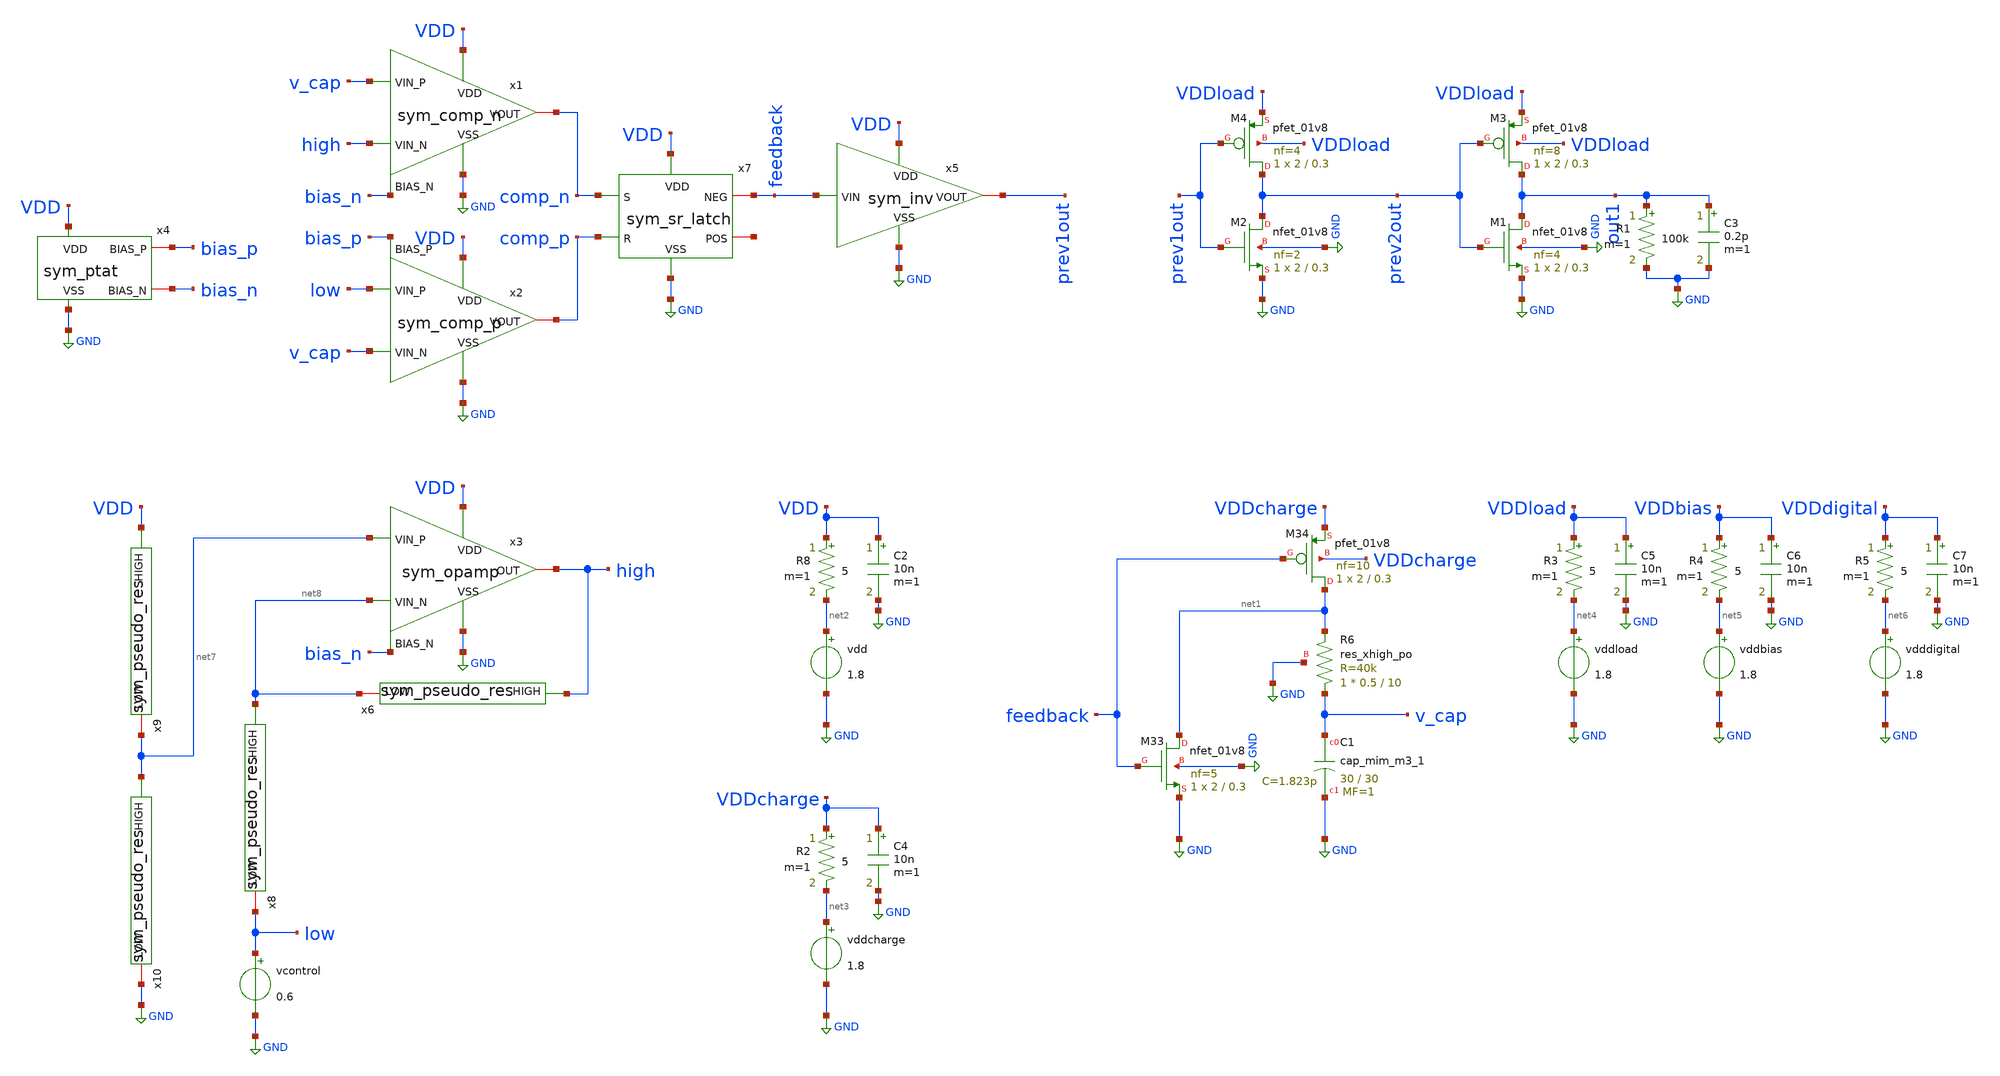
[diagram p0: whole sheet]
** sch_path: schem/tb/tb_full.sch
**.subckt tb_full
XC1 v_cap GND sky130_fd_pr__cap_mim_m3_1 W=30 L=30 MF=1 m=1
XM33 net1 feedback GND GND sky130_fd_pr__nfet_01v8 L=0.3 W=2 nf=5 ad='int((5 + 1)/2) * 2 / 5 * 0.29'
+ as='int((5 + 2)/2) * 2 / 5 * 0.29' pd='2*int((5 + 1)/2) * (2 / 5 + 0.29)' ps='2*int((5 + 2)/2) * (2 / 5 + 0.29)'
+ nrd='0.29 / 2 ' nrs='0.29 / 2 ' sa=0 sb=0 sd=0 mult=1 m=1
XM34 net1 feedback VDDcharge VDDcharge sky130_fd_pr__pfet_01v8 L=0.3 W=2 nf=10 ad='int((10 + 1)/2) * 2 / 10 * 0.29'
+ as='int((10 + 2)/2) * 2 / 10 * 0.29' pd='2*int((10 + 1)/2) * (2 / 10 + 0.29)' ps='2*int((10 + 2)/2) * (2 / 10 + 0.29)'
+ nrd='0.29 / 2 ' nrs='0.29 / 2 ' sa=0 sb=0 sd=0 mult=1 m=1
vdd net2 GND 1.8
C2 VDD GND 10n m=1
R8 VDD net2 5 m=1
vddcharge net3 GND 1.8
C4 VDDcharge GND 10n m=1
R2 VDDcharge net3 5 m=1
R1 out1 GND 100k m=1
C3 out1 GND 0.2p m=1
vddload net4 GND 1.8
C5 VDDload GND 10n m=1
R3 VDDload net4 5 m=1
vddbias net5 GND 1.8
C6 VDDbias GND 10n m=1
R4 VDDbias net5 5 m=1
vdddigital net6 GND 1.8
C7 VDDdigital GND 10n m=1
R5 VDDdigital net6 5 m=1
XM1 out1 prev2out GND GND sky130_fd_pr__nfet_01v8 L=0.3 W=2 nf=4 ad='int((4 + 1)/2) * 2 / 4 * 0.29' as='int((4 + 2)/2) * 2 / 4 * 0.29'
+ pd='2*int((4 + 1)/2) * (2 / 4 + 0.29)' ps='2*int((4 + 2)/2) * (2 / 4 + 0.29)' nrd='0.29 / 2 ' nrs='0.29 / 2 '
+ sa=0 sb=0 sd=0 mult=1 m=1
XM3 out1 prev2out VDDload VDDload sky130_fd_pr__pfet_01v8 L=0.3 W=2 nf=8 ad='int((8 + 1)/2) * 2 / 8 * 0.29'
+ as='int((8 + 2)/2) * 2 / 8 * 0.29' pd='2*int((8 + 1)/2) * (2 / 8 + 0.29)' ps='2*int((8 + 2)/2) * (2 / 8 + 0.29)'
+ nrd='0.29 / 2 ' nrs='0.29 / 2 ' sa=0 sb=0 sd=0 mult=1 m=1
XM2 prev2out prev1out GND GND sky130_fd_pr__nfet_01v8 L=0.3 W=2 nf=2 ad='int((2 + 1)/2) * 2 / 2 * 0.29'
+ as='int((2 + 2)/2) * 2 / 2 * 0.29' pd='2*int((2 + 1)/2) * (2 / 2 + 0.29)' ps='2*int((2 + 2)/2) * (2 / 2 + 0.29)'
+ nrd='0.29 / 2 ' nrs='0.29 / 2 ' sa=0 sb=0 sd=0 mult=1 m=1
XM4 prev2out prev1out VDDload VDDload sky130_fd_pr__pfet_01v8 L=0.3 W=2 nf=4 ad='int((4 + 1)/2) * 2 / 4 * 0.29'
+ as='int((4 + 2)/2) * 2 / 4 * 0.29' pd='2*int((4 + 1)/2) * (2 / 4 + 0.29)' ps='2*int((4 + 2)/2) * (2 / 4 + 0.29)'
+ nrd='0.29 / 2 ' nrs='0.29 / 2 ' sa=0 sb=0 sd=0 mult=1 m=1
XR6 v_cap net1 GND sky130_fd_pr__res_xhigh_po W=0.5 L=10 mult=1 m=1
vcontrol low GND 0.6
x4 VDD GND bias_p bias_n sym_ptat
x9 VDD net7 sym_pseudo_res
x10 net7 GND sym_pseudo_res
x8 net8 low sym_pseudo_res
x6 high net8 sym_pseudo_res
x3 VDD GND net7 net8 high bias_n sym_opamp
x1 VDD GND high v_cap comp_n bias_n sym_comp_n
x2 VDD GND bias_p comp_p low v_cap sym_comp_p
x5 VDD feedback prev1out GND sym_inv
x7 VDD GND comp_p comp_n feedback net9 sym_sr_latch
**** begin user architecture code


.lib /usr/local/share/pdk/sky130A/libs.tech/ngspice/sky130.lib.spice tt

.tran 0.1n 2u
.save all

.control
    run

    * Find rising edges of feedback signal (threshold at 0.9V for 1.8V signal)
    meas tran t1 when feedback=0.9 rise=2
    meas tran t2 when feedback=0.9 rise=3

    * Calculate period and frequency from 2nd period onwards
    let period = t2 - t1
    let freq = 1 / period

    print period
    print freq

    plot low high v_cap prev1out out1
    plot abs(i(vdd))*1.8 + abs(i(vddcharge))*1.8
.endc

.end


**** end user architecture code
**.ends

* expanding   symbol:  /home/zhixuan/projects/fyp_vco/schem/symbol_repo/sym_ptat.sym # of pins=4
** sym_path: schem/symbol_repo/sym_ptat.sym
** sch_path: schem/symbol_repo/sym_ptat.sch
.subckt sym_ptat VDD VSS BIAS_P BIAS_N
*.ipin VDD
*.ipin VSS
*.iopin BIAS_P
*.iopin BIAS_N
XMN_ptat2 net6 net1 net2 VSS sky130_fd_pr__nfet_01v8 L=0.5 W=2 nf=2 ad='int((2 + 1)/2) * 2 / 2 * 0.29'
+ as='int((2 + 2)/2) * 2 / 2 * 0.29' pd='2*int((2 + 1)/2) * (2 / 2 + 0.29)' ps='2*int((2 + 2)/2) * (2 / 2 + 0.29)'
+ nrd='0.29 / 2 ' nrs='0.29 / 2 ' sa=0 sb=0 sd=0 mult=1 m=1
XMP_diode1 net3 BIAS_P VDD VDD sky130_fd_pr__pfet_01v8 L=0.5 W=2 nf=2 ad='int((2 + 1)/2) * 2 / 2 * 0.29'
+ as='int((2 + 2)/2) * 2 / 2 * 0.29' pd='2*int((2 + 1)/2) * (2 / 2 + 0.29)' ps='2*int((2 + 2)/2) * (2 / 2 + 0.29)'
+ nrd='0.29 / 2 ' nrs='0.29 / 2 ' sa=0 sb=0 sd=0 mult=1 m=1
XMP_mir1_l net4 BIAS_P VDD VDD sky130_fd_pr__pfet_01v8 L=0.5 W=2 nf=2 ad='int((2 + 1)/2) * 2 / 2 * 0.29'
+ as='int((2 + 2)/2) * 2 / 2 * 0.29' pd='2*int((2 + 1)/2) * (2 / 2 + 0.29)' ps='2*int((2 + 2)/2) * (2 / 2 + 0.29)'
+ nrd='0.29 / 2 ' nrs='0.29 / 2 ' sa=0 sb=0 sd=0 mult=1 m=1
XMN_diode2 net5 net1 VSS VSS sky130_fd_pr__nfet_01v8 L=0.5 W=2 nf=4 ad='int((4 + 1)/2) * 2 / 4 * 0.29'
+ as='int((4 + 2)/2) * 2 / 4 * 0.29' pd='2*int((4 + 1)/2) * (2 / 4 + 0.29)' ps='2*int((4 + 2)/2) * (2 / 4 + 0.29)'
+ nrd='0.29 / 2 ' nrs='0.29 / 2 ' sa=0 sb=0 sd=0 mult=1 m=1
XMP_inv BIAS_N BIAS_P VDD VDD sky130_fd_pr__pfet_01v8 L=0.75 W=2 nf=5 ad='int((5 + 1)/2) * 2 / 5 * 0.29'
+ as='int((5 + 2)/2) * 2 / 5 * 0.29' pd='2*int((5 + 1)/2) * (2 / 5 + 0.29)' ps='2*int((5 + 2)/2) * (2 / 5 + 0.29)'
+ nrd='0.29 / 2 ' nrs='0.29 / 2 ' sa=0 sb=0 sd=0 mult=1 m=1
XMP_diode2 BIAS_P BIAS_P net3 VDD sky130_fd_pr__pfet_01v8 L=0.5 W=2 nf=2 ad='int((2 + 1)/2) * 2 / 2 * 0.29'
+ as='int((2 + 2)/2) * 2 / 2 * 0.29' pd='2*int((2 + 1)/2) * (2 / 2 + 0.29)' ps='2*int((2 + 2)/2) * (2 / 2 + 0.29)'
+ nrd='0.29 / 2 ' nrs='0.29 / 2 ' sa=0 sb=0 sd=0 mult=1 m=1
XMP_mir2_l net1 BIAS_P net4 VDD sky130_fd_pr__pfet_01v8 L=0.5 W=2 nf=2 ad='int((2 + 1)/2) * 2 / 2 * 0.29'
+ as='int((2 + 2)/2) * 2 / 2 * 0.29' pd='2*int((2 + 1)/2) * (2 / 2 + 0.29)' ps='2*int((2 + 2)/2) * (2 / 2 + 0.29)'
+ nrd='0.29 / 2 ' nrs='0.29 / 2 ' sa=0 sb=0 sd=0 mult=1 m=1
XMN_ptat1 BIAS_P net1 net6 VSS sky130_fd_pr__nfet_01v8 L=0.5 W=2 nf=2 ad='int((2 + 1)/2) * 2 / 2 * 0.29'
+ as='int((2 + 2)/2) * 2 / 2 * 0.29' pd='2*int((2 + 1)/2) * (2 / 2 + 0.29)' ps='2*int((2 + 2)/2) * (2 / 2 + 0.29)'
+ nrd='0.29 / 2 ' nrs='0.29 / 2 ' sa=0 sb=0 sd=0 mult=1 m=1
XMN_diode1 net1 net1 net5 VSS sky130_fd_pr__nfet_01v8 L=0.5 W=2 nf=4 ad='int((4 + 1)/2) * 2 / 4 * 0.29'
+ as='int((4 + 2)/2) * 2 / 4 * 0.29' pd='2*int((4 + 1)/2) * (2 / 4 + 0.29)' ps='2*int((4 + 2)/2) * (2 / 4 + 0.29)'
+ nrd='0.29 / 2 ' nrs='0.29 / 2 ' sa=0 sb=0 sd=0 mult=1 m=1
XMN_inv BIAS_N BIAS_N VSS VSS sky130_fd_pr__nfet_01v8 L=0.75 W=2.5 nf=2 ad='int((2 + 1)/2) * 2.5 / 2 * 0.29'
+ as='int((2 + 2)/2) * 2.5 / 2 * 0.29' pd='2*int((2 + 1)/2) * (2.5 / 2 + 0.29)' ps='2*int((2 + 2)/2) * (2.5 / 2 + 0.29)'
+ nrd='0.29 / 2.5 ' nrs='0.29 / 2.5 ' sa=0 sb=0 sd=0 mult=1 m=1
XR1 VSS net2 VSS sky130_fd_pr__res_xhigh_po_0p35 L=2.8 mult=1 m=1
XMP_startup net1 VSS VDD VDD sky130_fd_pr__pfet_01v8 L=13 W=1 nf=1 ad='int((1 + 1)/2) * 1 / 1 * 0.29'
+ as='int((1 + 2)/2) * 1 / 1 * 0.29' pd='2*int((1 + 1)/2) * (1 / 1 + 0.29)' ps='2*int((1 + 2)/2) * (1 / 1 + 0.29)'
+ nrd='0.29 / 1 ' nrs='0.29 / 1 ' sa=0 sb=0 sd=0 mult=1 m=1
XMN_diode3 net7 net1 VSS VSS sky130_fd_pr__nfet_01v8 L=0.5 W=2 nf=4 ad='int((4 + 1)/2) * 2 / 4 * 0.29'
+ as='int((4 + 2)/2) * 2 / 4 * 0.29' pd='2*int((4 + 1)/2) * (2 / 4 + 0.29)' ps='2*int((4 + 2)/2) * (2 / 4 + 0.29)'
+ nrd='0.29 / 2 ' nrs='0.29 / 2 ' sa=0 sb=0 sd=0 mult=1 m=1
XMN_diode4 net1 net1 net7 VSS sky130_fd_pr__nfet_01v8 L=0.5 W=2 nf=4 ad='int((4 + 1)/2) * 2 / 4 * 0.29'
+ as='int((4 + 2)/2) * 2 / 4 * 0.29' pd='2*int((4 + 1)/2) * (2 / 4 + 0.29)' ps='2*int((4 + 2)/2) * (2 / 4 + 0.29)'
+ nrd='0.29 / 2 ' nrs='0.29 / 2 ' sa=0 sb=0 sd=0 mult=1 m=1
.ends


* expanding   symbol:  /home/zhixuan/projects/fyp_vco/schem/symbol_repo/sym_pseudo_res.sym # of
*+ pins=2
** sym_path: schem/symbol_repo/sym_pseudo_res.sym
** sch_path: schem/symbol_repo/sym_pseudo_res.sch
.subckt sym_pseudo_res HIGH LOW
*.iopin LOW
*.ipin HIGH
XMP_r1 net1 net1 HIGH HIGH sky130_fd_pr__pfet_01v8 L=0.15 W=1 nf=1 ad='int((1 + 1)/2) * 1 / 1 * 0.29'
+ as='int((1 + 2)/2) * 1 / 1 * 0.29' pd='2*int((1 + 1)/2) * (1 / 1 + 0.29)' ps='2*int((1 + 2)/2) * (1 / 1 + 0.29)'
+ nrd='0.29 / 1 ' nrs='0.29 / 1 ' sa=0 sb=0 sd=0 mult=1 m=1
XMP_r2 LOW LOW net1 HIGH sky130_fd_pr__pfet_01v8 L=0.15 W=1 nf=1 ad='int((1 + 1)/2) * 1 / 1 * 0.29' as='int((1 + 2)/2) * 1 / 1 * 0.29'
+ pd='2*int((1 + 1)/2) * (1 / 1 + 0.29)' ps='2*int((1 + 2)/2) * (1 / 1 + 0.29)' nrd='0.29 / 1 ' nrs='0.29 / 1 '
+ sa=0 sb=0 sd=0 mult=1 m=1
.ends


* expanding   symbol:  /home/zhixuan/projects/fyp_vco/schem/symbol_repo/sym_opamp.sym # of pins=6
** sym_path: schem/symbol_repo/sym_opamp.sym
** sch_path: schem/symbol_repo/sym_opamp.sch
.subckt sym_opamp VDD VSS VIN_P VIN_N OUT BIAS_N
*.ipin VDD
*.ipin VSS
*.ipin BIAS_N
*.iopin OUT
*.ipin VIN_N
*.ipin VIN_P
XMN_vinn net1 VIN_N net3 VSS sky130_fd_pr__nfet_01v8 L=0.5 W=1 nf=1 ad='int((1 + 1)/2) * 1 / 1 * 0.29'
+ as='int((1 + 2)/2) * 1 / 1 * 0.29' pd='2*int((1 + 1)/2) * (1 / 1 + 0.29)' ps='2*int((1 + 2)/2) * (1 / 1 + 0.29)'
+ nrd='0.29 / 1 ' nrs='0.29 / 1 ' sa=0 sb=0 sd=0 mult=1 m=1
XMP_cs_1 net2 net1 VDD VDD sky130_fd_pr__pfet_01v8 L=0.5 W=2 nf=1 ad='int((1 + 1)/2) * 2 / 1 * 0.29'
+ as='int((1 + 2)/2) * 2 / 1 * 0.29' pd='2*int((1 + 1)/2) * (2 / 1 + 0.29)' ps='2*int((1 + 2)/2) * (2 / 1 + 0.29)'
+ nrd='0.29 / 2 ' nrs='0.29 / 2 ' sa=0 sb=0 sd=0 mult=1 m=1
XMP_diode net1 net1 VDD VDD sky130_fd_pr__pfet_01v8 L=0.5 W=2 nf=1 ad='int((1 + 1)/2) * 2 / 1 * 0.29'
+ as='int((1 + 2)/2) * 2 / 1 * 0.29' pd='2*int((1 + 1)/2) * (2 / 1 + 0.29)' ps='2*int((1 + 2)/2) * (2 / 1 + 0.29)'
+ nrd='0.29 / 2 ' nrs='0.29 / 2 ' sa=0 sb=0 sd=0 mult=1 m=1
XMN_vinp net2 VIN_P net3 VSS sky130_fd_pr__nfet_01v8 L=0.5 W=1 nf=1 ad='int((1 + 1)/2) * 1 / 1 * 0.29'
+ as='int((1 + 2)/2) * 1 / 1 * 0.29' pd='2*int((1 + 1)/2) * (1 / 1 + 0.29)' ps='2*int((1 + 2)/2) * (1 / 1 + 0.29)'
+ nrd='0.29 / 1 ' nrs='0.29 / 1 ' sa=0 sb=0 sd=0 mult=1 m=1
XMN_tail_1 net3 BIAS_N VSS GND sky130_fd_pr__nfet_01v8 L=0.75 W=2 nf=1 ad='int((1 + 1)/2) * 2 / 1 * 0.29'
+ as='int((1 + 2)/2) * 2 / 1 * 0.29' pd='2*int((1 + 1)/2) * (2 / 1 + 0.29)' ps='2*int((1 + 2)/2) * (2 / 1 + 0.29)'
+ nrd='0.29 / 2 ' nrs='0.29 / 2 ' sa=0 sb=0 sd=0 mult=1 m=1
XMP_cs_2 OUT net2 VDD VDD sky130_fd_pr__pfet_01v8 L=0.5 W=2 nf=1 ad='int((1 + 1)/2) * 2 / 1 * 0.29' as='int((1 + 2)/2) * 2 / 1 * 0.29'
+ pd='2*int((1 + 1)/2) * (2 / 1 + 0.29)' ps='2*int((1 + 2)/2) * (2 / 1 + 0.29)' nrd='0.29 / 2 ' nrs='0.29 / 2 '
+ sa=0 sb=0 sd=0 mult=1 m=1
XMN_tail_2 OUT BIAS_N VSS VSS sky130_fd_pr__nfet_01v8 L=0.75 W=2 nf=1 ad='int((1 + 1)/2) * 2 / 1 * 0.29'
+ as='int((1 + 2)/2) * 2 / 1 * 0.29' pd='2*int((1 + 1)/2) * (2 / 1 + 0.29)' ps='2*int((1 + 2)/2) * (2 / 1 + 0.29)'
+ nrd='0.29 / 2 ' nrs='0.29 / 2 ' sa=0 sb=0 sd=0 mult=1 m=1
XCc net4 OUT sky130_fd_pr__cap_mim_m3_1 W=4 L=4 MF=1 m=1
XR1 net4 net2 VSS sky130_fd_pr__res_xhigh_po_0p35 L=2 mult=1 m=1
.ends


* expanding   symbol:  /home/zhixuan/projects/fyp_vco/schem/symbol_repo/sym_comp_n.sym # of pins=6
** sym_path: schem/symbol_repo/sym_comp_n.sym
** sch_path: schem/symbol_repo/sym_comp_n.sch
.subckt sym_comp_n VDD VSS VIN_N VIN_P VOUT BIAS_N
*.ipin VDD
*.ipin VSS
*.ipin VIN_N
*.ipin VIN_P
*.ipin BIAS_N
*.iopin VOUT
XMP_diode_l net1 net1 VDD VDD sky130_fd_pr__pfet_01v8 L=0.3 W=2 nf=2 ad='int((2 + 1)/2) * 2 / 2 * 0.29'
+ as='int((2 + 2)/2) * 2 / 2 * 0.29' pd='2*int((2 + 1)/2) * (2 / 2 + 0.29)' ps='2*int((2 + 2)/2) * (2 / 2 + 0.29)'
+ nrd='0.29 / 2 ' nrs='0.29 / 2 ' sa=0 sb=0 sd=0 mult=1 m=1
XMP_cs_l net2 net1 VDD VDD sky130_fd_pr__pfet_01v8 L=0.3 W=2 nf=2 ad='int((2 + 1)/2) * 2 / 2 * 0.29'
+ as='int((2 + 2)/2) * 2 / 2 * 0.29' pd='2*int((2 + 1)/2) * (2 / 2 + 0.29)' ps='2*int((2 + 2)/2) * (2 / 2 + 0.29)'
+ nrd='0.29 / 2 ' nrs='0.29 / 2 ' sa=0 sb=0 sd=0 mult=1 m=1
XMP_cs_r net1 net2 VDD VDD sky130_fd_pr__pfet_01v8 L=0.3 W=2 nf=2 ad='int((2 + 1)/2) * 2 / 2 * 0.29'
+ as='int((2 + 2)/2) * 2 / 2 * 0.29' pd='2*int((2 + 1)/2) * (2 / 2 + 0.29)' ps='2*int((2 + 2)/2) * (2 / 2 + 0.29)'
+ nrd='0.29 / 2 ' nrs='0.29 / 2 ' sa=0 sb=0 sd=0 mult=1 m=1
XMP_diode_r net2 net2 VDD VDD sky130_fd_pr__pfet_01v8 L=0.3 W=2 nf=2 ad='int((2 + 1)/2) * 2 / 2 * 0.29'
+ as='int((2 + 2)/2) * 2 / 2 * 0.29' pd='2*int((2 + 1)/2) * (2 / 2 + 0.29)' ps='2*int((2 + 2)/2) * (2 / 2 + 0.29)'
+ nrd='0.29 / 2 ' nrs='0.29 / 2 ' sa=0 sb=0 sd=0 mult=1 m=1
XMN_vinn net1 VIN_N net3 VSS sky130_fd_pr__nfet_01v8 L=0.5 W=2.5 nf=1 ad='int((1 + 1)/2) * 2.5 / 1 * 0.29'
+ as='int((1 + 2)/2) * 2.5 / 1 * 0.29' pd='2*int((1 + 1)/2) * (2.5 / 1 + 0.29)' ps='2*int((1 + 2)/2) * (2.5 / 1 + 0.29)'
+ nrd='0.29 / 2.5 ' nrs='0.29 / 2.5 ' sa=0 sb=0 sd=0 mult=1 m=1
XMN_vinp net2 VIN_P net3 VSS sky130_fd_pr__nfet_01v8 L=0.5 W=2.5 nf=1 ad='int((1 + 1)/2) * 2.5 / 1 * 0.29'
+ as='int((1 + 2)/2) * 2.5 / 1 * 0.29' pd='2*int((1 + 1)/2) * (2.5 / 1 + 0.29)' ps='2*int((1 + 2)/2) * (2.5 / 1 + 0.29)'
+ nrd='0.29 / 2.5 ' nrs='0.29 / 2.5 ' sa=0 sb=0 sd=0 mult=1 m=1
XMN_tail net3 BIAS_N VSS VSS sky130_fd_pr__nfet_01v8 L=0.75 W=2.5 nf=2 ad='int((2 + 1)/2) * 2.5 / 2 * 0.29'
+ as='int((2 + 2)/2) * 2.5 / 2 * 0.29' pd='2*int((2 + 1)/2) * (2.5 / 2 + 0.29)' ps='2*int((2 + 2)/2) * (2.5 / 2 + 0.29)'
+ nrd='0.29 / 2.5 ' nrs='0.29 / 2.5 ' sa=0 sb=0 sd=0 mult=1 m=1
XMP_latch_r VOUT net2 VDD VDD sky130_fd_pr__pfet_01v8 L=0.15 W=0.5 nf=1 ad='int((1 + 1)/2) * 0.5 / 1 * 0.29'
+ as='int((1 + 2)/2) * 0.5 / 1 * 0.29' pd='2*int((1 + 1)/2) * (0.5 / 1 + 0.29)' ps='2*int((1 + 2)/2) * (0.5 / 1 + 0.29)'
+ nrd='0.29 / 0.5 ' nrs='0.29 / 0.5 ' sa=0 sb=0 sd=0 mult=1 m=1
XMP_latch_l net5 net1 VDD VDD sky130_fd_pr__pfet_01v8 L=0.15 W=0.5 nf=1 ad='int((1 + 1)/2) * 0.5 / 1 * 0.29'
+ as='int((1 + 2)/2) * 0.5 / 1 * 0.29' pd='2*int((1 + 1)/2) * (0.5 / 1 + 0.29)' ps='2*int((1 + 2)/2) * (0.5 / 1 + 0.29)'
+ nrd='0.29 / 0.5 ' nrs='0.29 / 0.5 ' sa=0 sb=0 sd=0 mult=1 m=1
XMN_latch_r VOUT net4 VSS VSS sky130_fd_pr__nfet_01v8 L=0.15 W=0.5 nf=1 ad='int((1 + 1)/2) * 0.5 / 1 * 0.29'
+ as='int((1 + 2)/2) * 0.5 / 1 * 0.29' pd='2*int((1 + 1)/2) * (0.5 / 1 + 0.29)' ps='2*int((1 + 2)/2) * (0.5 / 1 + 0.29)'
+ nrd='0.29 / 0.5 ' nrs='0.29 / 0.5 ' sa=0 sb=0 sd=0 mult=1 m=1
XMN_diode_l net4 net4 VSS VSS sky130_fd_pr__nfet_01v8 L=0.15 W=0.5 nf=1 ad='int((1 + 1)/2) * 0.5 / 1 * 0.29'
+ as='int((1 + 2)/2) * 0.5 / 1 * 0.29' pd='2*int((1 + 1)/2) * (0.5 / 1 + 0.29)' ps='2*int((1 + 2)/2) * (0.5 / 1 + 0.29)'
+ nrd='0.29 / 0.5 ' nrs='0.29 / 0.5 ' sa=0 sb=0 sd=0 mult=1 m=1
XMP_lim net4 net4 net5 VDD sky130_fd_pr__pfet_01v8 L=0.15 W=0.5 nf=1 ad='int((1 + 1)/2) * 0.5 / 1 * 0.29'
+ as='int((1 + 2)/2) * 0.5 / 1 * 0.29' pd='2*int((1 + 1)/2) * (0.5 / 1 + 0.29)' ps='2*int((1 + 2)/2) * (0.5 / 1 + 0.29)'
+ nrd='0.29 / 0.5 ' nrs='0.29 / 0.5 ' sa=0 sb=0 sd=0 mult=1 m=1
.ends


* expanding   symbol:  /home/zhixuan/projects/fyp_vco/schem/symbol_repo/sym_comp_p.sym # of pins=6
** sym_path: schem/symbol_repo/sym_comp_p.sym
** sch_path: schem/symbol_repo/sym_comp_p.sch
.subckt sym_comp_p VDD VSS BIAS_P VOUT VIN_P VIN_N
*.ipin VDD
*.ipin VSS
*.ipin BIAS_P
*.ipin VIN_N
*.ipin VIN_P
*.iopin VOUT
XMN_cs_l net2 net1 VSS VSS sky130_fd_pr__nfet_01v8 L=0.15 W=1 nf=1 ad='int((1 + 1)/2) * 1 / 1 * 0.29'
+ as='int((1 + 2)/2) * 1 / 1 * 0.29' pd='2*int((1 + 1)/2) * (1 / 1 + 0.29)' ps='2*int((1 + 2)/2) * (1 / 1 + 0.29)'
+ nrd='0.29 / 1 ' nrs='0.29 / 1 ' sa=0 sb=0 sd=0 mult=1 m=1
XMP_tail net4 BIAS_P VDD VDD sky130_fd_pr__pfet_01v8 L=0.75 W=2 nf=5 ad='int((5 + 1)/2) * 2 / 5 * 0.29'
+ as='int((5 + 2)/2) * 2 / 5 * 0.29' pd='2*int((5 + 1)/2) * (2 / 5 + 0.29)' ps='2*int((5 + 2)/2) * (2 / 5 + 0.29)'
+ nrd='0.29 / 2 ' nrs='0.29 / 2 ' sa=0 sb=0 sd=0 mult=1 m=1
XMP_vinn net1 VIN_N net4 VDD sky130_fd_pr__pfet_01v8 L=0.5 W=2.5 nf=2 ad='int((2 + 1)/2) * 2.5 / 2 * 0.29'
+ as='int((2 + 2)/2) * 2.5 / 2 * 0.29' pd='2*int((2 + 1)/2) * (2.5 / 2 + 0.29)' ps='2*int((2 + 2)/2) * (2.5 / 2 + 0.29)'
+ nrd='0.29 / 2.5 ' nrs='0.29 / 2.5 ' sa=0 sb=0 sd=0 mult=1 m=1
XMP_vinp net2 VIN_P net4 VDD sky130_fd_pr__pfet_01v8 L=0.5 W=2.5 nf=2 ad='int((2 + 1)/2) * 2.5 / 2 * 0.29'
+ as='int((2 + 2)/2) * 2.5 / 2 * 0.29' pd='2*int((2 + 1)/2) * (2.5 / 2 + 0.29)' ps='2*int((2 + 2)/2) * (2.5 / 2 + 0.29)'
+ nrd='0.29 / 2.5 ' nrs='0.29 / 2.5 ' sa=0 sb=0 sd=0 mult=1 m=1
XMN_diode_l net1 net1 VSS VSS sky130_fd_pr__nfet_01v8 L=0.15 W=1 nf=1 ad='int((1 + 1)/2) * 1 / 1 * 0.29'
+ as='int((1 + 2)/2) * 1 / 1 * 0.29' pd='2*int((1 + 1)/2) * (1 / 1 + 0.29)' ps='2*int((1 + 2)/2) * (1 / 1 + 0.29)'
+ nrd='0.29 / 1 ' nrs='0.29 / 1 ' sa=0 sb=0 sd=0 mult=1 m=1
XMN_diode_r net2 net2 VSS VSS sky130_fd_pr__nfet_01v8 L=0.15 W=1 nf=1 ad='int((1 + 1)/2) * 1 / 1 * 0.29'
+ as='int((1 + 2)/2) * 1 / 1 * 0.29' pd='2*int((1 + 1)/2) * (1 / 1 + 0.29)' ps='2*int((1 + 2)/2) * (1 / 1 + 0.29)'
+ nrd='0.29 / 1 ' nrs='0.29 / 1 ' sa=0 sb=0 sd=0 mult=1 m=1
XMN_cs_r net1 net2 VSS VSS sky130_fd_pr__nfet_01v8 L=0.15 W=1 nf=1 ad='int((1 + 1)/2) * 1 / 1 * 0.29'
+ as='int((1 + 2)/2) * 1 / 1 * 0.29' pd='2*int((1 + 1)/2) * (1 / 1 + 0.29)' ps='2*int((1 + 2)/2) * (1 / 1 + 0.29)'
+ nrd='0.29 / 1 ' nrs='0.29 / 1 ' sa=0 sb=0 sd=0 mult=1 m=1
XMN_latch_l net5 net1 VSS VSS sky130_fd_pr__nfet_01v8 L=0.15 W=0.5 nf=1 ad='int((1 + 1)/2) * 0.5 / 1 * 0.29'
+ as='int((1 + 2)/2) * 0.5 / 1 * 0.29' pd='2*int((1 + 1)/2) * (0.5 / 1 + 0.29)' ps='2*int((1 + 2)/2) * (0.5 / 1 + 0.29)'
+ nrd='0.29 / 0.5 ' nrs='0.29 / 0.5 ' sa=0 sb=0 sd=0 mult=1 m=1
XMN_latch_r VOUT net2 VSS VSS sky130_fd_pr__nfet_01v8 L=0.15 W=0.5 nf=1 ad='int((1 + 1)/2) * 0.5 / 1 * 0.29'
+ as='int((1 + 2)/2) * 0.5 / 1 * 0.29' pd='2*int((1 + 1)/2) * (0.5 / 1 + 0.29)' ps='2*int((1 + 2)/2) * (0.5 / 1 + 0.29)'
+ nrd='0.29 / 0.5 ' nrs='0.29 / 0.5 ' sa=0 sb=0 sd=0 mult=1 m=1
XMP_diode_l net3 net3 VDD VDD sky130_fd_pr__pfet_01v8 L=0.15 W=0.5 nf=1 ad='int((1 + 1)/2) * 0.5 / 1 * 0.29'
+ as='int((1 + 2)/2) * 0.5 / 1 * 0.29' pd='2*int((1 + 1)/2) * (0.5 / 1 + 0.29)' ps='2*int((1 + 2)/2) * (0.5 / 1 + 0.29)'
+ nrd='0.29 / 0.5 ' nrs='0.29 / 0.5 ' sa=0 sb=0 sd=0 mult=1 m=1
XMP_latch_r VOUT net3 VDD VDD sky130_fd_pr__pfet_01v8 L=0.15 W=0.5 nf=1 ad='int((1 + 1)/2) * 0.5 / 1 * 0.29'
+ as='int((1 + 2)/2) * 0.5 / 1 * 0.29' pd='2*int((1 + 1)/2) * (0.5 / 1 + 0.29)' ps='2*int((1 + 2)/2) * (0.5 / 1 + 0.29)'
+ nrd='0.29 / 0.5 ' nrs='0.29 / 0.5 ' sa=0 sb=0 sd=0 mult=1 m=1
XMP_lim net5 net5 net3 VDD sky130_fd_pr__pfet_01v8 L=0.15 W=0.5 nf=1 ad='int((1 + 1)/2) * 0.5 / 1 * 0.29'
+ as='int((1 + 2)/2) * 0.5 / 1 * 0.29' pd='2*int((1 + 1)/2) * (0.5 / 1 + 0.29)' ps='2*int((1 + 2)/2) * (0.5 / 1 + 0.29)'
+ nrd='0.29 / 0.5 ' nrs='0.29 / 0.5 ' sa=0 sb=0 sd=0 mult=1 m=1
.ends


* expanding   symbol:  /home/zhixuan/projects/fyp_vco/schem/symbol_repo/sym_inv.sym # of pins=4
** sym_path: schem/symbol_repo/sym_inv.sym
** sch_path: schem/symbol_repo/sym_inv.sch
.subckt sym_inv VDD VIN VOUT VSS
*.ipin VIN
*.ipin VDD
*.ipin VSS
*.iopin VOUT
XMN_pldwn VOUT VIN VSS VSS sky130_fd_pr__nfet_01v8 L=0.15 W=1 nf=1 ad='int((1 + 1)/2) * 1 / 1 * 0.29'
+ as='int((1 + 2)/2) * 1 / 1 * 0.29' pd='2*int((1 + 1)/2) * (1 / 1 + 0.29)' ps='2*int((1 + 2)/2) * (1 / 1 + 0.29)'
+ nrd='0.29 / 1 ' nrs='0.29 / 1 ' sa=0 sb=0 sd=0 mult=1 m=1
XMP_plup VOUT VIN VDD VDD sky130_fd_pr__pfet_01v8 L=0.15 W=2 nf=1 ad='int((1 + 1)/2) * 2 / 1 * 0.29'
+ as='int((1 + 2)/2) * 2 / 1 * 0.29' pd='2*int((1 + 1)/2) * (2 / 1 + 0.29)' ps='2*int((1 + 2)/2) * (2 / 1 + 0.29)'
+ nrd='0.29 / 2 ' nrs='0.29 / 2 ' sa=0 sb=0 sd=0 mult=1 m=1
.ends


* expanding   symbol:  /home/zhixuan/projects/fyp_vco/schem/symbol_repo/sym_sr_latch.sym # of pins=6
** sym_path: schem/symbol_repo/sym_sr_latch.sym
** sch_path: schem/symbol_repo/sym_sr_latch.sch
.subckt sym_sr_latch VDD VSS R S NEG POS
*.ipin S
*.ipin VDD
*.ipin R
*.ipin VSS
*.iopin POS
*.iopin NEG
XMN_neg POS NEG VSS VSS sky130_fd_pr__nfet_01v8 L=0.15 W=1 nf=1 ad='int((1 + 1)/2) * 1 / 1 * 0.29' as='int((1 + 2)/2) * 1 / 1 * 0.29'
+ pd='2*int((1 + 1)/2) * (1 / 1 + 0.29)' ps='2*int((1 + 2)/2) * (1 / 1 + 0.29)' nrd='0.29 / 1 ' nrs='0.29 / 1 '
+ sa=0 sb=0 sd=0 mult=1 m=1
XMP_s net1 S VDD VDD sky130_fd_pr__pfet_01v8 L=0.15 W=2 nf=1 ad='int((1 + 1)/2) * 2 / 1 * 0.29' as='int((1 + 2)/2) * 2 / 1 * 0.29'
+ pd='2*int((1 + 1)/2) * (2 / 1 + 0.29)' ps='2*int((1 + 2)/2) * (2 / 1 + 0.29)' nrd='0.29 / 2 ' nrs='0.29 / 2 '
+ sa=0 sb=0 sd=0 mult=1 m=1
XMP_neg POS NEG net1 VDD sky130_fd_pr__pfet_01v8 L=0.15 W=2 nf=1 ad='int((1 + 1)/2) * 2 / 1 * 0.29' as='int((1 + 2)/2) * 2 / 1 * 0.29'
+ pd='2*int((1 + 1)/2) * (2 / 1 + 0.29)' ps='2*int((1 + 2)/2) * (2 / 1 + 0.29)' nrd='0.29 / 2 ' nrs='0.29 / 2 '
+ sa=0 sb=0 sd=0 mult=1 m=1
XMN_s POS S VSS VSS sky130_fd_pr__nfet_01v8 L=0.15 W=1 nf=1 ad='int((1 + 1)/2) * 1 / 1 * 0.29' as='int((1 + 2)/2) * 1 / 1 * 0.29'
+ pd='2*int((1 + 1)/2) * (1 / 1 + 0.29)' ps='2*int((1 + 2)/2) * (1 / 1 + 0.29)' nrd='0.29 / 1 ' nrs='0.29 / 1 '
+ sa=0 sb=0 sd=0 mult=1 m=1
XMN_r NEG R VSS VSS sky130_fd_pr__nfet_01v8 L=0.15 W=1 nf=1 ad='int((1 + 1)/2) * 1 / 1 * 0.29' as='int((1 + 2)/2) * 1 / 1 * 0.29'
+ pd='2*int((1 + 1)/2) * (1 / 1 + 0.29)' ps='2*int((1 + 2)/2) * (1 / 1 + 0.29)' nrd='0.29 / 1 ' nrs='0.29 / 1 '
+ sa=0 sb=0 sd=0 mult=1 m=1
XMP_r net2 R VDD VDD sky130_fd_pr__pfet_01v8 L=0.15 W=2 nf=1 ad='int((1 + 1)/2) * 2 / 1 * 0.29' as='int((1 + 2)/2) * 2 / 1 * 0.29'
+ pd='2*int((1 + 1)/2) * (2 / 1 + 0.29)' ps='2*int((1 + 2)/2) * (2 / 1 + 0.29)' nrd='0.29 / 2 ' nrs='0.29 / 2 '
+ sa=0 sb=0 sd=0 mult=1 m=1
XMP_pos NEG POS net2 VDD sky130_fd_pr__pfet_01v8 L=0.15 W=2 nf=1 ad='int((1 + 1)/2) * 2 / 1 * 0.29' as='int((1 + 2)/2) * 2 / 1 * 0.29'
+ pd='2*int((1 + 1)/2) * (2 / 1 + 0.29)' ps='2*int((1 + 2)/2) * (2 / 1 + 0.29)' nrd='0.29 / 2 ' nrs='0.29 / 2 '
+ sa=0 sb=0 sd=0 mult=1 m=1
XMN_pos NEG POS VSS VSS sky130_fd_pr__nfet_01v8 L=0.15 W=1 nf=1 ad='int((1 + 1)/2) * 1 / 1 * 0.29' as='int((1 + 2)/2) * 1 / 1 * 0.29'
+ pd='2*int((1 + 1)/2) * (1 / 1 + 0.29)' ps='2*int((1 + 2)/2) * (1 / 1 + 0.29)' nrd='0.29 / 1 ' nrs='0.29 / 1 '
+ sa=0 sb=0 sd=0 mult=1 m=1
.ends

.GLOBAL GND
.end
